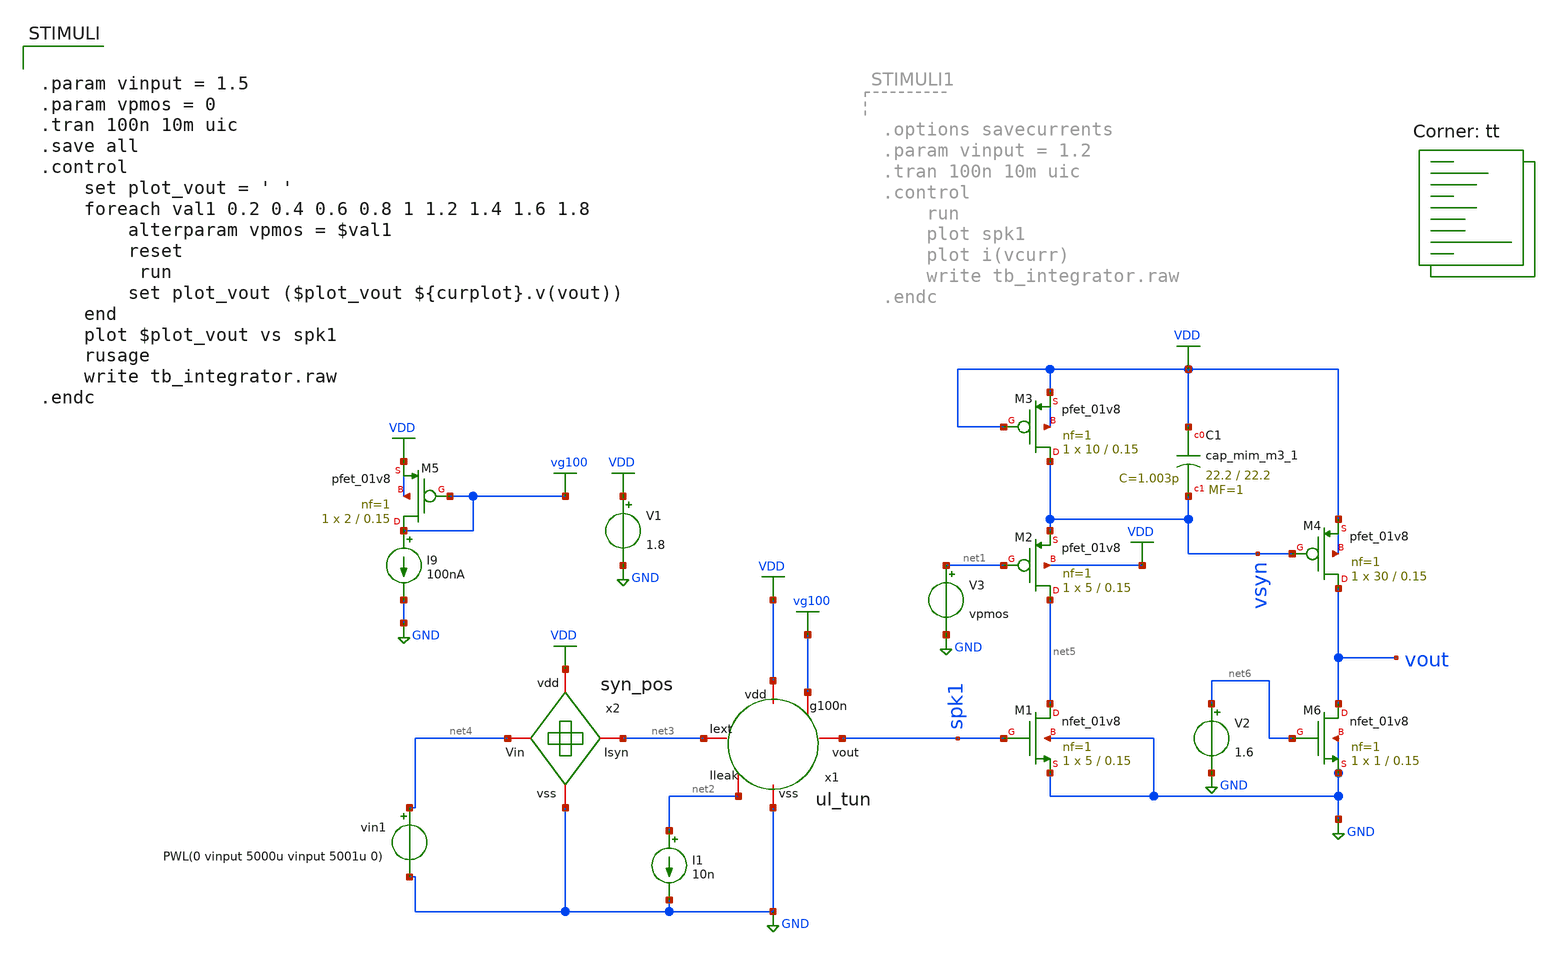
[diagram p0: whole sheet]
** sch_path: Neuron/ultralif/tb_integrator.sch
**.subckt tb_integrator
XM1 net5 spk1 GND GND sky130_fd_pr__nfet_01v8 L=0.15 W=5 nf=1 ad='int((nf+1)/2) * W/nf * 0.29' as='int((nf+2)/2) * W/nf * 0.29'
+ pd='2*int((nf+1)/2) * (W/nf + 0.29)' ps='2*int((nf+2)/2) * (W/nf + 0.29)' nrd='0.29 / W' nrs='0.29 / W'
+ sa=0 sb=0 sd=0 mult=1 m=1
XM2 net5 net1 vsyn VDD sky130_fd_pr__pfet_01v8 L=0.15 W=5 nf=1 ad='int((nf+1)/2) * W/nf * 0.29' as='int((nf+2)/2) * W/nf * 0.29'
+ pd='2*int((nf+1)/2) * (W/nf + 0.29)' ps='2*int((nf+2)/2) * (W/nf + 0.29)' nrd='0.29 / W' nrs='0.29 / W'
+ sa=0 sb=0 sd=0 mult=1 m=1
XM3 vsyn VDD VDD VDD sky130_fd_pr__pfet_01v8 L=0.15 W=10 nf=1 ad='int((nf+1)/2) * W/nf * 0.29' as='int((nf+2)/2) * W/nf * 0.29'
+ pd='2*int((nf+1)/2) * (W/nf + 0.29)' ps='2*int((nf+2)/2) * (W/nf + 0.29)' nrd='0.29 / W' nrs='0.29 / W'
+ sa=0 sb=0 sd=0 mult=1 m=1
XM4 vout vsyn VDD VDD sky130_fd_pr__pfet_01v8 L=0.15 W=30 nf=1 ad='int((nf+1)/2) * W/nf * 0.29' as='int((nf+2)/2) * W/nf * 0.29'
+ pd='2*int((nf+1)/2) * (W/nf + 0.29)' ps='2*int((nf+2)/2) * (W/nf + 0.29)' nrd='0.29 / W' nrs='0.29 / W'
+ sa=0 sb=0 sd=0 mult=1 m=1
XC1 VDD vsyn sky130_fd_pr__cap_mim_m3_1 W=22.2 L=22.2 MF=1 m=1
V1 VDD GND 1.8
I1 net2 GND 10n
x1 net3 VDD vg100 spk1 net2 GND ul_tun
I9 vg100 GND 100nA
XM5 vg100 vg100 VDD VDD sky130_fd_pr__pfet_01v8 L=0.15 W=2 nf=1 ad='int((nf+1)/2) * W/nf * 0.29' as='int((nf+2)/2) * W/nf * 0.29'
+ pd='2*int((nf+1)/2) * (W/nf + 0.29)' ps='2*int((nf+2)/2) * (W/nf + 0.29)' nrd='0.29 / W' nrs='0.29 / W'
+ sa=0 sb=0 sd=0 mult=1 m=1
vin1 net4 GND PWL(0 vinput 5000u vinput 5001u 0)
x2 VDD net4 net3 GND syn_pos
XM6 vout net6 GND GND sky130_fd_pr__nfet_01v8 L=0.15 W=1 nf=1 ad='int((nf+1)/2) * W/nf * 0.29' as='int((nf+2)/2) * W/nf * 0.29'
+ pd='2*int((nf+1)/2) * (W/nf + 0.29)' ps='2*int((nf+2)/2) * (W/nf + 0.29)' nrd='0.29 / W' nrs='0.29 / W'
+ sa=0 sb=0 sd=0 mult=1 m=1
V2 net6 GND 1.6
V3 net1 GND vpmos
**** begin user architecture code
.lib $::SKYWATER_MODELS/sky130.lib.spice tt
**** end user architecture code
**.ends

* expanding   symbol:  ul_tun.sym # of pins=6
** sym_path: Neuron/ultralif/ul_tun.sym
** sch_path: Neuron/ultralif/ul_tun.sch
.subckt ul_tun Iext vdd g100n vout Ileak vss
*.iopin Iext
*.iopin vout
*.iopin vss
*.iopin Ileak
*.iopin vdd
*.iopin g100n
XM1 Ileak Ileak net1 vdd sky130_fd_pr__pfet_01v8 L=10 W=1 nf=1 ad='int((nf+1)/2) * W/nf * 0.29' as='int((nf+2)/2) * W/nf * 0.29'
+ pd='2*int((nf+1)/2) * (W/nf + 0.29)' ps='2*int((nf+2)/2) * (W/nf + 0.29)' nrd='0.29 / W' nrs='0.29 / W'
+ sa=0 sb=0 sd=0 mult=1 m=1
XM2 Ileak net2 net1 vdd sky130_fd_pr__pfet_01v8 L=0.15 W=1.5 nf=1 ad='int((nf+1)/2) * W/nf * 0.29' as='int((nf+2)/2) * W/nf * 0.29'
+ pd='2*int((nf+1)/2) * (W/nf + 0.29)' ps='2*int((nf+2)/2) * (W/nf + 0.29)' nrd='0.29 / W' nrs='0.29 / W'
+ sa=0 sb=0 sd=0 mult=1 m=1
XM3 net2 net2 net1 vdd sky130_fd_pr__pfet_01v8 L=0.15 W=15 nf=1 ad='int((nf+1)/2) * W/nf * 0.29' as='int((nf+2)/2) * W/nf * 0.29'
+ pd='2*int((nf+1)/2) * (W/nf + 0.29)' ps='2*int((nf+2)/2) * (W/nf + 0.29)' nrd='0.29 / W' nrs='0.29 / W'
+ sa=0 sb=0 sd=0 mult=1 m=1
XM4 net2 Ileak vss vss sky130_fd_pr__nfet_01v8 L=4 W=1 nf=1 ad='int((1 + 1)/2) * 1 / 1 * 0.29' as='int((1 + 2)/2) * 1 / 1 * 0.29'
+ pd='2*int((1 + 1)/2) * (1 / 1 + 0.29)' ps='2*int((1 + 2)/2) * (1 / 1 + 0.29)' nrd='0.29 / 1 ' nrs='0.29 / 1 '
+ sa=0 sb=0 sd=0 mult=1 m=1
C1 net1 vss 1p m=1
XM5 vout_n Ileak vss vss sky130_fd_pr__nfet_01v8 L=0.15 W=1 nf=1 ad='int((1 + 1)/2) * 1 / 1 * 0.29' as='int((1 + 2)/2) * 1 / 1 * 0.29'
+ pd='2*int((1 + 1)/2) * (1 / 1 + 0.29)' ps='2*int((1 + 2)/2) * (1 / 1 + 0.29)' nrd='0.29 / 1 ' nrs='0.29 / 1 '
+ sa=0 sb=0 sd=0 mult=1 m=1
XM6 vout_n g100n vdd vdd sky130_fd_pr__pfet_01v8 L=0.15 W=2 nf=1 ad='int((nf+1)/2) * W/nf * 0.29' as='int((nf+2)/2) * W/nf * 0.29'
+ pd='2*int((nf+1)/2) * (W/nf + 0.29)' ps='2*int((nf+2)/2) * (W/nf + 0.29)' nrd='0.29 / W' nrs='0.29 / W'
+ sa=0 sb=0 sd=0 mult=1 m=1
XM7 vout vout_n vss vss sky130_fd_pr__nfet_01v8 L=0.15 W=1 nf=1 ad='int((1 + 1)/2) * 1 / 1 * 0.29' as='int((1 + 2)/2) * 1 / 1 * 0.29'
+ pd='2*int((1 + 1)/2) * (1 / 1 + 0.29)' ps='2*int((1 + 2)/2) * (1 / 1 + 0.29)' nrd='0.29 / 1 ' nrs='0.29 / 1 '
+ sa=0 sb=0 sd=0 mult=1 m=1
XM8 vout vout_n vdd vdd sky130_fd_pr__pfet_01v8 L=0.15 W=2 nf=1 ad='int((nf+1)/2) * W/nf * 0.29' as='int((nf+2)/2) * W/nf * 0.29'
+ pd='2*int((nf+1)/2) * (W/nf + 0.29)' ps='2*int((nf+2)/2) * (W/nf + 0.29)' nrd='0.29 / W' nrs='0.29 / W'
+ sa=0 sb=0 sd=0 mult=1 m=1
vext Iext net1 0
**** begin user architecture code


.save i(vext)


**** end user architecture code
.ends


* expanding   symbol:  syn_pos.sym # of pins=4
** sym_path: Neuron/ultralif/syn_pos.sym
** sch_path: Neuron/ultralif/syn_pos.sch
.subckt syn_pos vdd Vin Isyn vss
*.iopin Vin
*.iopin vdd
*.iopin vss
*.iopin Isyn
XM9 Isyn vx vdd vdd sky130_fd_pr__pfet_01v8 L=1 W=0.5 nf=1 ad='int((nf+1)/2) * W/nf * 0.29' as='int((nf+2)/2) * W/nf * 0.29'
+ pd='2*int((nf+1)/2) * (W/nf + 0.29)' ps='2*int((nf+2)/2) * (W/nf + 0.29)' nrd='0.29 / W' nrs='0.29 / W'
+ sa=0 sb=0 sd=0 mult=1 m=1
XM10 vx vx vdd vdd sky130_fd_pr__pfet_01v8 L=0.15 W=0.5 nf=1 ad='int((nf+1)/2) * W/nf * 0.29' as='int((nf+2)/2) * W/nf * 0.29'
+ pd='2*int((nf+1)/2) * (W/nf + 0.29)' ps='2*int((nf+2)/2) * (W/nf + 0.29)' nrd='0.29 / W' nrs='0.29 / W'
+ sa=0 sb=0 sd=0 mult=5 m=5
XM12 vx Vin vss vss sky130_fd_pr__nfet_01v8 L=1 W=0.4 nf=1 ad='int((1 + 1)/2) * 0.4 / 1 * 0.29' as='int((1 + 2)/2) * 0.4 / 1 * 0.29'
+ pd='2*int((1 + 1)/2) * (0.4 / 1 + 0.29)' ps='2*int((1 + 2)/2) * (0.4 / 1 + 0.29)' nrd='0.29 / 0.4 ' nrs='0.29 / 0.4 '
+ sa=0 sb=0 sd=0 mult=1 m=1
.ends

.GLOBAL GND
.GLOBAL VDD
.GLOBAL vg100
**** begin user architecture code


.param vinput = 1.5
.param vpmos = 0
.tran 100n 10m uic
.save all
.control
	set plot_vout = ' '
	foreach val1 0.2 0.4 0.6 0.8 1 1.2 1.4 1.6 1.8
		alterparam vpmos = $val1
		reset
	 	run
		set plot_vout ($plot_vout ${curplot}.v(vout))
	end
	plot $plot_vout vs spk1
	rusage
	write tb_integrator.raw
.endc


**** end user architecture code
.end
